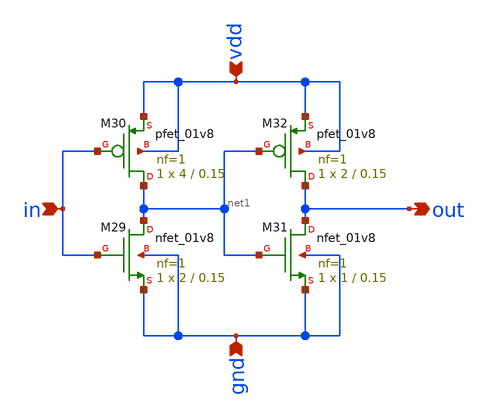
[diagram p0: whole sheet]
** sch_path: Projects/Schematic_Design_and_Analysis_of_an_8-Word_8-Bit_Static_RAM_with_6T_Storage_Cells_using_SKY130PDK/assets/schematic/buffer.sch
**.subckt buffer in vdd gnd out
*.ipin in
*.ipin vdd
*.ipin gnd
*.opin out
XM29 net1 in gnd gnd sky130_fd_pr__nfet_01v8 L=0.15 W=2 nf=1 ad='int((nf+1)/2) * W/nf * 0.29' as='int((nf+2)/2) * W/nf * 0.29'
+ pd='2*int((nf+1)/2) * (W/nf + 0.29)' ps='2*int((nf+2)/2) * (W/nf + 0.29)' nrd='0.29 / W' nrs='0.29 / W'
+ sa=0 sb=0 sd=0 mult=1 m=1
XM30 net1 in vdd vdd sky130_fd_pr__pfet_01v8 L=0.15 W=4 nf=1 ad='int((nf+1)/2) * W/nf * 0.29' as='int((nf+2)/2) * W/nf * 0.29'
+ pd='2*int((nf+1)/2) * (W/nf + 0.29)' ps='2*int((nf+2)/2) * (W/nf + 0.29)' nrd='0.29 / W' nrs='0.29 / W'
+ sa=0 sb=0 sd=0 mult=1 m=1
XM31 out net1 gnd gnd sky130_fd_pr__nfet_01v8 L=0.15 W=1 nf=1 ad='int((nf+1)/2) * W/nf * 0.29' as='int((nf+2)/2) * W/nf * 0.29'
+ pd='2*int((nf+1)/2) * (W/nf + 0.29)' ps='2*int((nf+2)/2) * (W/nf + 0.29)' nrd='0.29 / W' nrs='0.29 / W'
+ sa=0 sb=0 sd=0 mult=1 m=1
XM32 out net1 vdd vdd sky130_fd_pr__pfet_01v8 L=0.15 W=2 nf=1 ad='int((nf+1)/2) * W/nf * 0.29' as='int((nf+2)/2) * W/nf * 0.29'
+ pd='2*int((nf+1)/2) * (W/nf + 0.29)' ps='2*int((nf+2)/2) * (W/nf + 0.29)' nrd='0.29 / W' nrs='0.29 / W'
+ sa=0 sb=0 sd=0 mult=1 m=1
**.ends
.end
